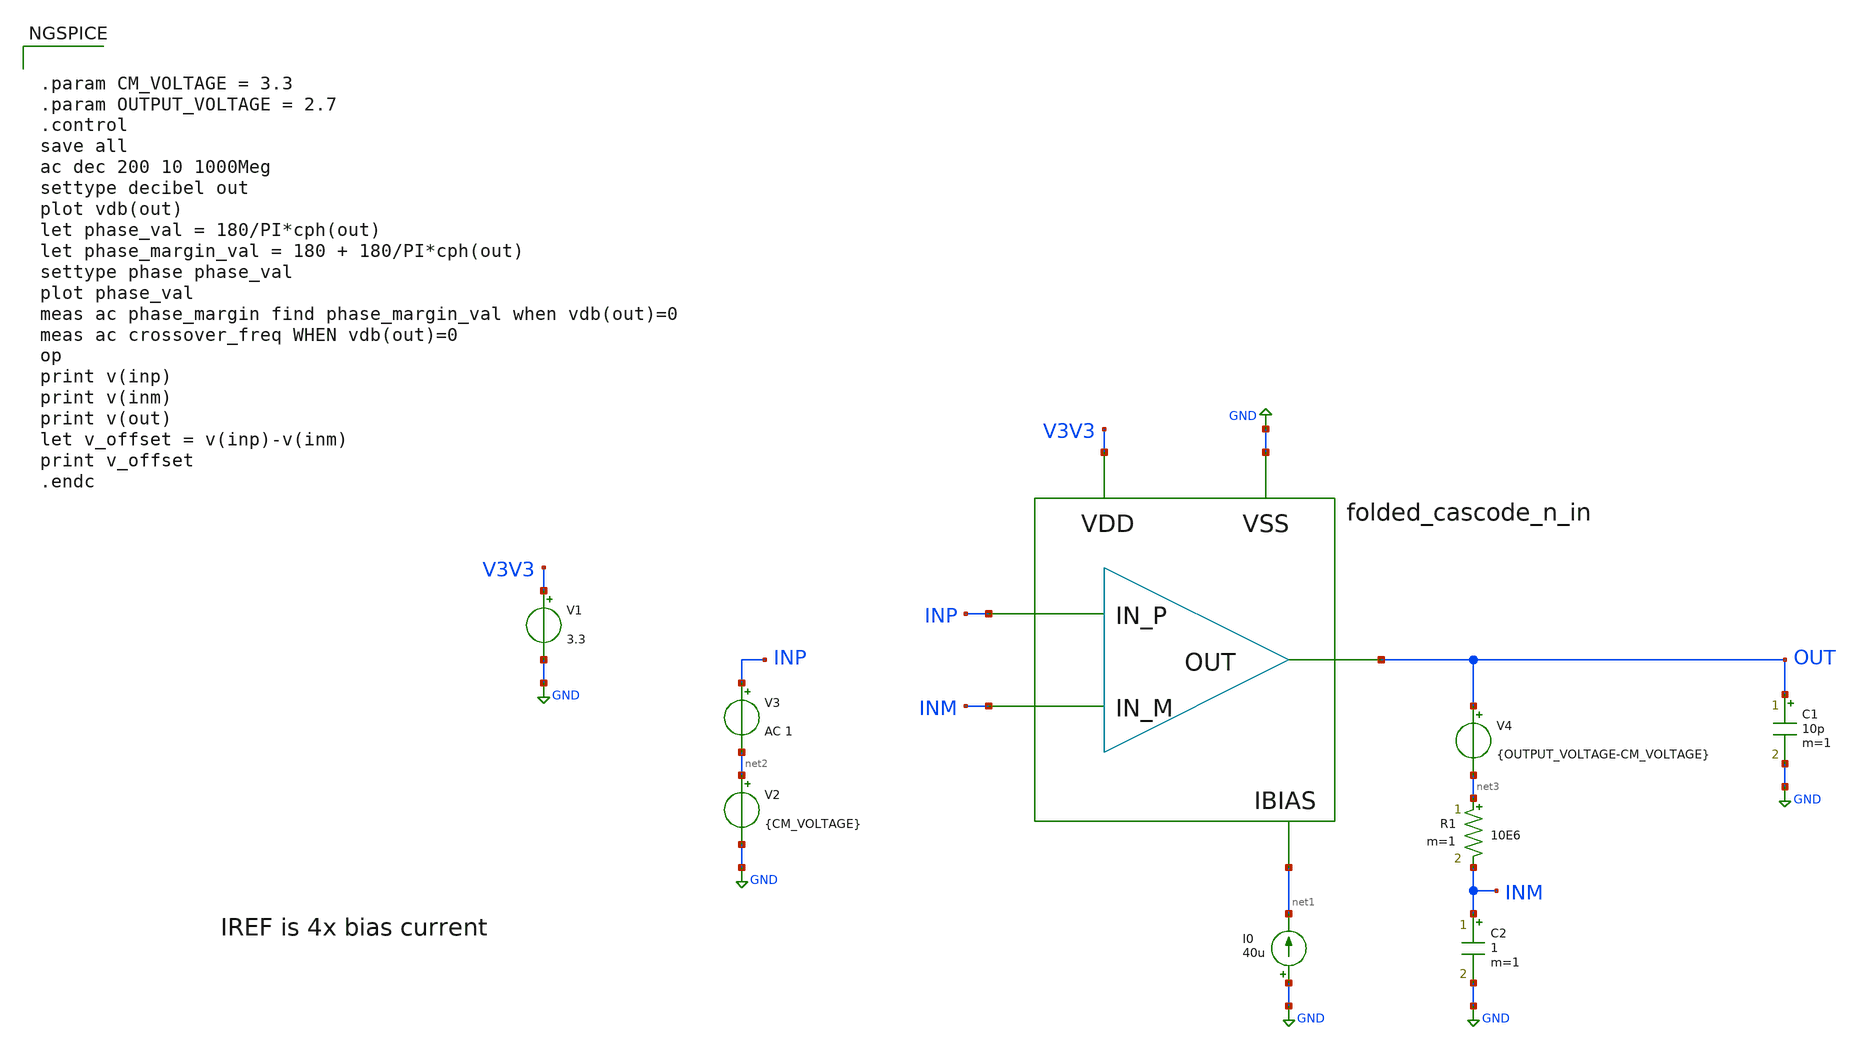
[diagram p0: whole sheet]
** sch_path: design/folded-cascode-n-in/folded_cascode_n_in_tb.sch
**.subckt folded_cascode_n_in_tb
V1 V3V3 GND 3.3
I0 GND net1 40u
x1 INP INM OUT V3V3 GND net1 folded_cascode_n_in
V2 net2 GND {CM_VOLTAGE}
V3 INP net2 AC 1
C1 OUT GND 10p m=1
R1 net3 INM 10E6 m=1
V4 OUT net3 {OUTPUT_VOLTAGE-CM_VOLTAGE}
C2 INM GND 1 m=1
**** begin user architecture code


.param CM_VOLTAGE = 3.3
.param OUTPUT_VOLTAGE = 2.7
.control
save all
ac dec 200 10 1000Meg
settype decibel out
plot vdb(out)
let phase_val = 180/PI*cph(out)
let phase_margin_val = 180 + 180/PI*cph(out)
settype phase phase_val
plot phase_val
meas ac phase_margin find phase_margin_val when vdb(out)=0
meas ac crossover_freq WHEN vdb(out)=0
op
print v(inp)
print v(inm)
print v(out)
let v_offset = v(inp)-v(inm)
print v_offset
.endc



.include $::SKYWATER_MODELS/cells/nfet_01v8/sky130_fd_pr__nfet_01v8__tt.corner.spice
.include $::SKYWATER_MODELS/cells/nfet_01v8_lvt/sky130_fd_pr__nfet_01v8_lvt__tt.corner.spice
.include $::SKYWATER_MODELS/cells/pfet_01v8/sky130_fd_pr__pfet_01v8__tt.corner.spice
.include $::SKYWATER_MODELS/cells/nfet_03v3_nvt/sky130_fd_pr__nfet_03v3_nvt__tt.corner.spice
.include $::SKYWATER_MODELS/cells/nfet_05v0_nvt/sky130_fd_pr__nfet_05v0_nvt__tt.corner.spice
.include $::SKYWATER_MODELS/cells/esd_nfet_01v8/sky130_fd_pr__esd_nfet_01v8__tt.corner.spice
.include $::SKYWATER_MODELS/cells/pfet_01v8_lvt/sky130_fd_pr__pfet_01v8_lvt__tt.corner.spice
.include $::SKYWATER_MODELS/cells/pfet_01v8_hvt/sky130_fd_pr__pfet_01v8_hvt__tt.corner.spice
.include $::SKYWATER_MODELS/cells/esd_pfet_g5v0d10v5/sky130_fd_pr__esd_pfet_g5v0d10v5__tt.corner.spice
.include $::SKYWATER_MODELS/cells/pfet_g5v0d10v5/sky130_fd_pr__pfet_g5v0d10v5__tt.corner.spice
.include $::SKYWATER_MODELS/cells/pfet_g5v0d16v0/sky130_fd_pr__pfet_g5v0d16v0__tt.corner.spice
.include $::SKYWATER_MODELS/cells/nfet_g5v0d10v5/sky130_fd_pr__nfet_g5v0d10v5__tt.corner.spice
.include $::SKYWATER_MODELS/cells/nfet_g5v0d16v0/sky130_fd_pr__nfet_g5v0d16v0__tt_discrete.corner.spice
.include $::SKYWATER_MODELS/cells/esd_nfet_g5v0d10v5/sky130_fd_pr__esd_nfet_g5v0d10v5__tt.corner.spice
.include $::SKYWATER_MODELS/models/corners/tt/nonfet.spice
* Mismatch parameters
.include $::SKYWATER_MODELS/cells/nfet_01v8/sky130_fd_pr__nfet_01v8__mismatch.corner.spice
.include $::SKYWATER_MODELS/cells/pfet_01v8/sky130_fd_pr__pfet_01v8__mismatch.corner.spice
.include $::SKYWATER_MODELS/cells/nfet_01v8_lvt/sky130_fd_pr__nfet_01v8_lvt__mismatch.corner.spice
.include $::SKYWATER_MODELS/cells/pfet_01v8_lvt/sky130_fd_pr__pfet_01v8_lvt__mismatch.corner.spice
.include $::SKYWATER_MODELS/cells/pfet_01v8_hvt/sky130_fd_pr__pfet_01v8_hvt__mismatch.corner.spice
.include $::SKYWATER_MODELS/cells/nfet_g5v0d10v5/sky130_fd_pr__nfet_g5v0d10v5__mismatch.corner.spice
.include $::SKYWATER_MODELS/cells/pfet_g5v0d10v5/sky130_fd_pr__pfet_g5v0d10v5__mismatch.corner.spice
.include $::SKYWATER_MODELS/cells/nfet_05v0_nvt/sky130_fd_pr__nfet_05v0_nvt__mismatch.corner.spice
.include $::SKYWATER_MODELS/cells/nfet_03v3_nvt/sky130_fd_pr__nfet_03v3_nvt__mismatch.corner.spice
* Resistor$::SKYWATER_MODELS/Capacitor
.include $::SKYWATER_MODELS/models/r+c/res_typical__cap_typical.spice
.include $::SKYWATER_MODELS/models/r+c/res_typical__cap_typical__lin.spice
* Special cells
.include $::SKYWATER_MODELS/models/corners/tt/specialized_cells.spice
* All models
.include $::SKYWATER_MODELS/models/all.spice
* Corner
.include $::SKYWATER_MODELS/models/corners/tt/rf.spice

**** end user architecture code
**.ends

* expanding   symbol:  design/folded-cascode-n-in/folded_cascode_n_in.sym # of pins=6
** sym_path: design/folded-cascode-n-in/folded_cascode_n_in.sym
** sch_path: design/folded-cascode-n-in/folded_cascode_n_in.sch
.subckt folded_cascode_n_in IN_P IN_M OUT VDD VSS VBN
*.ipin IN_P
*.ipin IN_M
*.ipin OUT
*.ipin VDD
*.ipin VSS
*.ipin VBN
XM1 net1 VBN VSS VSS sky130_fd_pr__nfet_g5v0d10v5 L=1 W=5 nf=1 ad='int((nf+1)/2) * W/nf * 0.29' as='int((nf+2)/2) * W/nf * 0.29'
+ pd='2*int((nf+1)/2) * (W/nf + 0.29)' ps='2*int((nf+2)/2) * (W/nf + 0.29)' nrd='0.29 / W' nrs='0.29 / W'
+ sa=0 sb=0 sd=0 mult=12 m=12
XM3 VS1_P IN_M net1 VSS sky130_fd_pr__nfet_g5v0d10v5 L=1 W=5 nf=1 ad='int((nf+1)/2) * W/nf * 0.29' as='int((nf+2)/2) * W/nf * 0.29'
+ pd='2*int((nf+1)/2) * (W/nf + 0.29)' ps='2*int((nf+2)/2) * (W/nf + 0.29)' nrd='0.29 / W' nrs='0.29 / W'
+ sa=0 sb=0 sd=0 mult=24 m=24
XM4 VS1_M IN_P net1 VSS sky130_fd_pr__nfet_g5v0d10v5 L=1 W=5 nf=1 ad='int((nf+1)/2) * W/nf * 0.29' as='int((nf+2)/2) * W/nf * 0.29'
+ pd='2*int((nf+1)/2) * (W/nf + 0.29)' ps='2*int((nf+2)/2) * (W/nf + 0.29)' nrd='0.29 / W' nrs='0.29 / W'
+ sa=0 sb=0 sd=0 mult=24 m=24
XM9 net2 VCN net4 VSS sky130_fd_pr__nfet_g5v0d10v5 L=1 W=5 nf=1 ad='int((nf+1)/2) * W/nf * 0.29' as='int((nf+2)/2) * W/nf * 0.29'
+ pd='2*int((nf+1)/2) * (W/nf + 0.29)' ps='2*int((nf+2)/2) * (W/nf + 0.29)' nrd='0.29 / W' nrs='0.29 / W'
+ sa=0 sb=0 sd=0 mult=3 m=3
XM10 net3 net2 VSS VSS sky130_fd_pr__nfet_g5v0d10v5 L=1 W=5 nf=1 ad='int((nf+1)/2) * W/nf * 0.29' as='int((nf+2)/2) * W/nf * 0.29'
+ pd='2*int((nf+1)/2) * (W/nf + 0.29)' ps='2*int((nf+2)/2) * (W/nf + 0.29)' nrd='0.29 / W' nrs='0.29 / W'
+ sa=0 sb=0 sd=0 mult=3 m=3
XM11 net4 net2 VSS VSS sky130_fd_pr__nfet_g5v0d10v5 L=1 W=5 nf=1 ad='int((nf+1)/2) * W/nf * 0.29' as='int((nf+2)/2) * W/nf * 0.29'
+ pd='2*int((nf+1)/2) * (W/nf + 0.29)' ps='2*int((nf+2)/2) * (W/nf + 0.29)' nrd='0.29 / W' nrs='0.29 / W'
+ sa=0 sb=0 sd=0 mult=3 m=3
XM12 OUT VCN net3 VSS sky130_fd_pr__nfet_g5v0d10v5 L=1 W=5 nf=1 ad='int((nf+1)/2) * W/nf * 0.29' as='int((nf+2)/2) * W/nf * 0.29'
+ pd='2*int((nf+1)/2) * (W/nf + 0.29)' ps='2*int((nf+2)/2) * (W/nf + 0.29)' nrd='0.29 / W' nrs='0.29 / W'
+ sa=0 sb=0 sd=0 mult=3 m=3
XM5 VS1_P VBP_INT VDD VDD sky130_fd_pr__pfet_g5v0d10v5 L=1 W=5 nf=1 ad='int((nf+1)/2) * W/nf * 0.29'
+ as='int((nf+2)/2) * W/nf * 0.29' pd='2*int((nf+1)/2) * (W/nf + 0.29)' ps='2*int((nf+2)/2) * (W/nf + 0.29)'
+ nrd='0.29 / W' nrs='0.29 / W' sa=0 sb=0 sd=0 mult=9 m=9
XM13 VS1_M VBP_INT VDD VDD sky130_fd_pr__pfet_g5v0d10v5 L=1 W=5 nf=1 ad='int((nf+1)/2) * W/nf * 0.29'
+ as='int((nf+2)/2) * W/nf * 0.29' pd='2*int((nf+1)/2) * (W/nf + 0.29)' ps='2*int((nf+2)/2) * (W/nf + 0.29)'
+ nrd='0.29 / W' nrs='0.29 / W' sa=0 sb=0 sd=0 mult=9 m=9
XM17 VBP_INT VBN VSS VSS sky130_fd_pr__nfet_g5v0d10v5 L=1 W=5 nf=1 ad='int((nf+1)/2) * W/nf * 0.29' as='int((nf+2)/2) * W/nf * 0.29'
+ pd='2*int((nf+1)/2) * (W/nf + 0.29)' ps='2*int((nf+2)/2) * (W/nf + 0.29)' nrd='0.29 / W' nrs='0.29 / W'
+ sa=0 sb=0 sd=0 mult=1 m=1
XM18 VBP_INT VBP_INT VDD VDD sky130_fd_pr__pfet_g5v0d10v5 L=1 W=5 nf=1 ad='int((nf+1)/2) * W/nf * 0.29'
+ as='int((nf+2)/2) * W/nf * 0.29' pd='2*int((nf+1)/2) * (W/nf + 0.29)' ps='2*int((nf+2)/2) * (W/nf + 0.29)'
+ nrd='0.29 / W' nrs='0.29 / W' sa=0 sb=0 sd=0 mult=1 m=1
XM14 net2 VCP VS1_M VDD sky130_fd_pr__pfet_g5v0d10v5 L=1 W=5 nf=1 ad='int((nf+1)/2) * W/nf * 0.29' as='int((nf+2)/2) * W/nf * 0.29'
+ pd='2*int((nf+1)/2) * (W/nf + 0.29)' ps='2*int((nf+2)/2) * (W/nf + 0.29)' nrd='0.29 / W' nrs='0.29 / W'
+ sa=0 sb=0 sd=0 mult=3 m=3
XM19 OUT VCP VS1_P VDD sky130_fd_pr__pfet_g5v0d10v5 L=1 W=5 nf=1 ad='int((nf+1)/2) * W/nf * 0.29' as='int((nf+2)/2) * W/nf * 0.29'
+ pd='2*int((nf+1)/2) * (W/nf + 0.29)' ps='2*int((nf+2)/2) * (W/nf + 0.29)' nrd='0.29 / W' nrs='0.29 / W'
+ sa=0 sb=0 sd=0 mult=3 m=3
XM2 VBP_INT VBP_INT VS1_P VSS sky130_fd_pr__nfet_g5v0d10v5 L=1 W=5 nf=1 ad='int((nf+1)/2) * W/nf * 0.29'
+ as='int((nf+2)/2) * W/nf * 0.29' pd='2*int((nf+1)/2) * (W/nf + 0.29)' ps='2*int((nf+2)/2) * (W/nf + 0.29)'
+ nrd='0.29 / W' nrs='0.29 / W' sa=0 sb=0 sd=0 mult=1 m=1
XM6 VBP_INT VBP_INT VS1_M VSS sky130_fd_pr__nfet_g5v0d10v5 L=1 W=5 nf=1 ad='int((nf+1)/2) * W/nf * 0.29'
+ as='int((nf+2)/2) * W/nf * 0.29' pd='2*int((nf+1)/2) * (W/nf + 0.29)' ps='2*int((nf+2)/2) * (W/nf + 0.29)'
+ nrd='0.29 / W' nrs='0.29 / W' sa=0 sb=0 sd=0 mult=1 m=1
XM7 VBP VBP VDD VDD sky130_fd_pr__pfet_g5v0d10v5 L=1 W=5 nf=1 ad='int((nf+1)/2) * W/nf * 0.29' as='int((nf+2)/2) * W/nf * 0.29'
+ pd='2*int((nf+1)/2) * (W/nf + 0.29)' ps='2*int((nf+2)/2) * (W/nf + 0.29)' nrd='0.29 / W' nrs='0.29 / W'
+ sa=0 sb=0 sd=0 mult=1 m=1
XM8 net5 VBP net12 VDD sky130_fd_pr__pfet_g5v0d10v5 L=1 W=5 nf=1 ad='int((nf+1)/2) * W/nf * 0.29' as='int((nf+2)/2) * W/nf * 0.29'
+ pd='2*int((nf+1)/2) * (W/nf + 0.29)' ps='2*int((nf+2)/2) * (W/nf + 0.29)' nrd='0.29 / W' nrs='0.29 / W'
+ sa=0 sb=0 sd=0 mult=1 m=1
XM15 VCN VBP VDD VDD sky130_fd_pr__pfet_g5v0d10v5 L=1 W=5 nf=1 ad='int((nf+1)/2) * W/nf * 0.29' as='int((nf+2)/2) * W/nf * 0.29'
+ pd='2*int((nf+1)/2) * (W/nf + 0.29)' ps='2*int((nf+2)/2) * (W/nf + 0.29)' nrd='0.29 / W' nrs='0.29 / W'
+ sa=0 sb=0 sd=0 mult=1 m=1
XM16 net5 net5 net6 VSS sky130_fd_pr__nfet_g5v0d10v5 L=1 W=5 nf=1 ad='int((nf+1)/2) * W/nf * 0.29' as='int((nf+2)/2) * W/nf * 0.29'
+ pd='2*int((nf+1)/2) * (W/nf + 0.29)' ps='2*int((nf+2)/2) * (W/nf + 0.29)' nrd='0.29 / W' nrs='0.29 / W'
+ sa=0 sb=0 sd=0 mult=2 m=2
XM20 net6 net5 VSS VSS sky130_fd_pr__nfet_g5v0d10v5 L=1 W=5 nf=1 ad='int((nf+1)/2) * W/nf * 0.29' as='int((nf+2)/2) * W/nf * 0.29'
+ pd='2*int((nf+1)/2) * (W/nf + 0.29)' ps='2*int((nf+2)/2) * (W/nf + 0.29)' nrd='0.29 / W' nrs='0.29 / W'
+ sa=0 sb=0 sd=0 mult=1 m=1
XM21 VCN VCN net6 VSS sky130_fd_pr__nfet_g5v0d10v5 L=1 W=5 nf=1 ad='int((nf+1)/2) * W/nf * 0.29' as='int((nf+2)/2) * W/nf * 0.29'
+ pd='2*int((nf+1)/2) * (W/nf + 0.29)' ps='2*int((nf+2)/2) * (W/nf + 0.29)' nrd='0.29 / W' nrs='0.29 / W'
+ sa=0 sb=0 sd=0 mult=1 m=1
XM24 net7 VBN net10 VSS sky130_fd_pr__nfet_g5v0d10v5 L=1 W=5 nf=1 ad='int((nf+1)/2) * W/nf * 0.29' as='int((nf+2)/2) * W/nf * 0.29'
+ pd='2*int((nf+1)/2) * (W/nf + 0.29)' ps='2*int((nf+2)/2) * (W/nf + 0.29)' nrd='0.29 / W' nrs='0.29 / W'
+ sa=0 sb=0 sd=0 mult=1 m=1
XM25 VCP VBN VSS VSS sky130_fd_pr__nfet_g5v0d10v5 L=1 W=5 nf=1 ad='int((nf+1)/2) * W/nf * 0.29' as='int((nf+2)/2) * W/nf * 0.29'
+ pd='2*int((nf+1)/2) * (W/nf + 0.29)' ps='2*int((nf+2)/2) * (W/nf + 0.29)' nrd='0.29 / W' nrs='0.29 / W'
+ sa=0 sb=0 sd=0 mult=1 m=1
XM26 net7 net7 net8 VDD sky130_fd_pr__pfet_g5v0d10v5 L=1 W=5 nf=1 ad='int((nf+1)/2) * W/nf * 0.29' as='int((nf+2)/2) * W/nf * 0.29'
+ pd='2*int((nf+1)/2) * (W/nf + 0.29)' ps='2*int((nf+2)/2) * (W/nf + 0.29)' nrd='0.29 / W' nrs='0.29 / W'
+ sa=0 sb=0 sd=0 mult=2 m=2
XM27 VCP VCP net8 VDD sky130_fd_pr__pfet_g5v0d10v5 L=1 W=5 nf=1 ad='int((nf+1)/2) * W/nf * 0.29' as='int((nf+2)/2) * W/nf * 0.29'
+ pd='2*int((nf+1)/2) * (W/nf + 0.29)' ps='2*int((nf+2)/2) * (W/nf + 0.29)' nrd='0.29 / W' nrs='0.29 / W'
+ sa=0 sb=0 sd=0 mult=1 m=1
XM28 net8 net7 VDD VDD sky130_fd_pr__pfet_g5v0d10v5 L=1 W=5 nf=1 ad='int((nf+1)/2) * W/nf * 0.29' as='int((nf+2)/2) * W/nf * 0.29'
+ pd='2*int((nf+1)/2) * (W/nf + 0.29)' ps='2*int((nf+2)/2) * (W/nf + 0.29)' nrd='0.29 / W' nrs='0.29 / W'
+ sa=0 sb=0 sd=0 mult=1 m=1
XM29 VBP VBN VSS VSS sky130_fd_pr__nfet_g5v0d10v5 L=1 W=5 nf=1 ad='int((nf+1)/2) * W/nf * 0.29' as='int((nf+2)/2) * W/nf * 0.29'
+ pd='2*int((nf+1)/2) * (W/nf + 0.29)' ps='2*int((nf+2)/2) * (W/nf + 0.29)' nrd='0.29 / W' nrs='0.29 / W'
+ sa=0 sb=0 sd=0 mult=1 m=1
XM32 net12 VBP net9 VDD sky130_fd_pr__pfet_g5v0d10v5 L=1 W=5 nf=1 ad='int((nf+1)/2) * W/nf * 0.29' as='int((nf+2)/2) * W/nf * 0.29'
+ pd='2*int((nf+1)/2) * (W/nf + 0.29)' ps='2*int((nf+2)/2) * (W/nf + 0.29)' nrd='0.29 / W' nrs='0.29 / W'
+ sa=0 sb=0 sd=0 mult=1 m=1
XM33 net9 VBP VDD VDD sky130_fd_pr__pfet_g5v0d10v5 L=1 W=5 nf=1 ad='int((nf+1)/2) * W/nf * 0.29' as='int((nf+2)/2) * W/nf * 0.29'
+ pd='2*int((nf+1)/2) * (W/nf + 0.29)' ps='2*int((nf+2)/2) * (W/nf + 0.29)' nrd='0.29 / W' nrs='0.29 / W'
+ sa=0 sb=0 sd=0 mult=1 m=1
XM34 net10 VBN net11 VSS sky130_fd_pr__nfet_g5v0d10v5 L=1 W=5 nf=1 ad='int((nf+1)/2) * W/nf * 0.29' as='int((nf+2)/2) * W/nf * 0.29'
+ pd='2*int((nf+1)/2) * (W/nf + 0.29)' ps='2*int((nf+2)/2) * (W/nf + 0.29)' nrd='0.29 / W' nrs='0.29 / W'
+ sa=0 sb=0 sd=0 mult=1 m=1
XM35 net11 VBN VSS VSS sky130_fd_pr__nfet_g5v0d10v5 L=1 W=5 nf=1 ad='int((nf+1)/2) * W/nf * 0.29' as='int((nf+2)/2) * W/nf * 0.29'
+ pd='2*int((nf+1)/2) * (W/nf + 0.29)' ps='2*int((nf+2)/2) * (W/nf + 0.29)' nrd='0.29 / W' nrs='0.29 / W'
+ sa=0 sb=0 sd=0 mult=1 m=1
XM30 VBN VBN VSS VSS sky130_fd_pr__nfet_g5v0d10v5 L=1 W=5 nf=1 ad='int((nf+1)/2) * W/nf * 0.29' as='int((nf+2)/2) * W/nf * 0.29'
+ pd='2*int((nf+1)/2) * (W/nf + 0.29)' ps='2*int((nf+2)/2) * (W/nf + 0.29)' nrd='0.29 / W' nrs='0.29 / W'
+ sa=0 sb=0 sd=0 mult=1 m=1
.ends

.GLOBAL GND
**** begin user architecture code
[sky130_models]
**** end user architecture code
.end
